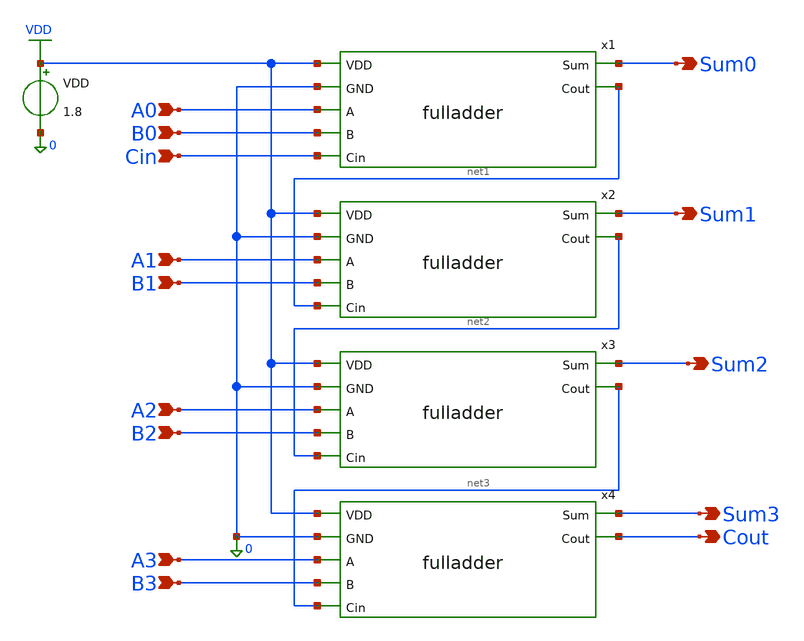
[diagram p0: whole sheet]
** sch_path: static_cmos/testbench/fa4_tb_tran.sch
**.subckt fa4_tb_tran Sum0 Sum1 Sum2 Sum3 Cout A0 B0 Cin A1 B1 B2 A2 B3 A3
*.opin Sum0
*.opin Sum1
*.opin Sum2
*.opin Sum3
*.opin Cout
*.ipin A0
*.ipin B0
*.ipin Cin
*.ipin A1
*.ipin B1
*.ipin B2
*.ipin A2
*.ipin B3
*.ipin A3
x1 VDD 0 Sum0 A0 B0 Cin net1 fulladder
x2 VDD 0 Sum1 A1 B1 net1 net2 fulladder
x3 VDD 0 Sum2 A2 B2 net2 net3 fulladder
x4 VDD 0 Sum3 A3 B3 net3 Cout fulladder
VDD VDD 0 1.8
**** begin user architecture code


.lib /usr/local/share/pdk/sky130A/libs.tech/ngspice/sky130.lib.spice tt
Va0  a0  0 pulse(0 1.8 1n   100p 100p 0.8n   2n)
Va1  a1  0 pulse(0 1.8 2n   100p 100p 1.8n   4n)
Va2  a2  0 pulse(0 1.8 4n   100p 100p 3.8n   8n)
Va3  a3  0 pulse(0 1.8 8n   100p 100p 7.8n   16n)
Vb0  b0  0 pulse(0 1.8 16n  100p 100p 15.8n  32n)
Vb1  b1  0 pulse(0 1.8 32n  100p 100p 31.8n  64n)
Vb2  b2  0 pulse(0 1.8 64n  100p 100p 63.8n  128n)
Vb3  b3  0 pulse(0 1.8 128n 100p 100p 127.8n 256n)
Vcin cin 0 pulse(0 1.8 256n 100p 100p 255.8n 512n)
.tran 10p 512n
.control
run
plot v(Cin) v(a3)-2 v(a2)-4 v(a1)-6 v(a0)-8 v(b3)-10 v(b2)-12 v(b1)-14 v(b0)-16 v(sum3)-18
+ v(sum2)-20 v(sum1)-22 v(sum0)-24 v(cout)-26
.endc


**** end user architecture code
**.ends
.GLOBAL VDD
.end
